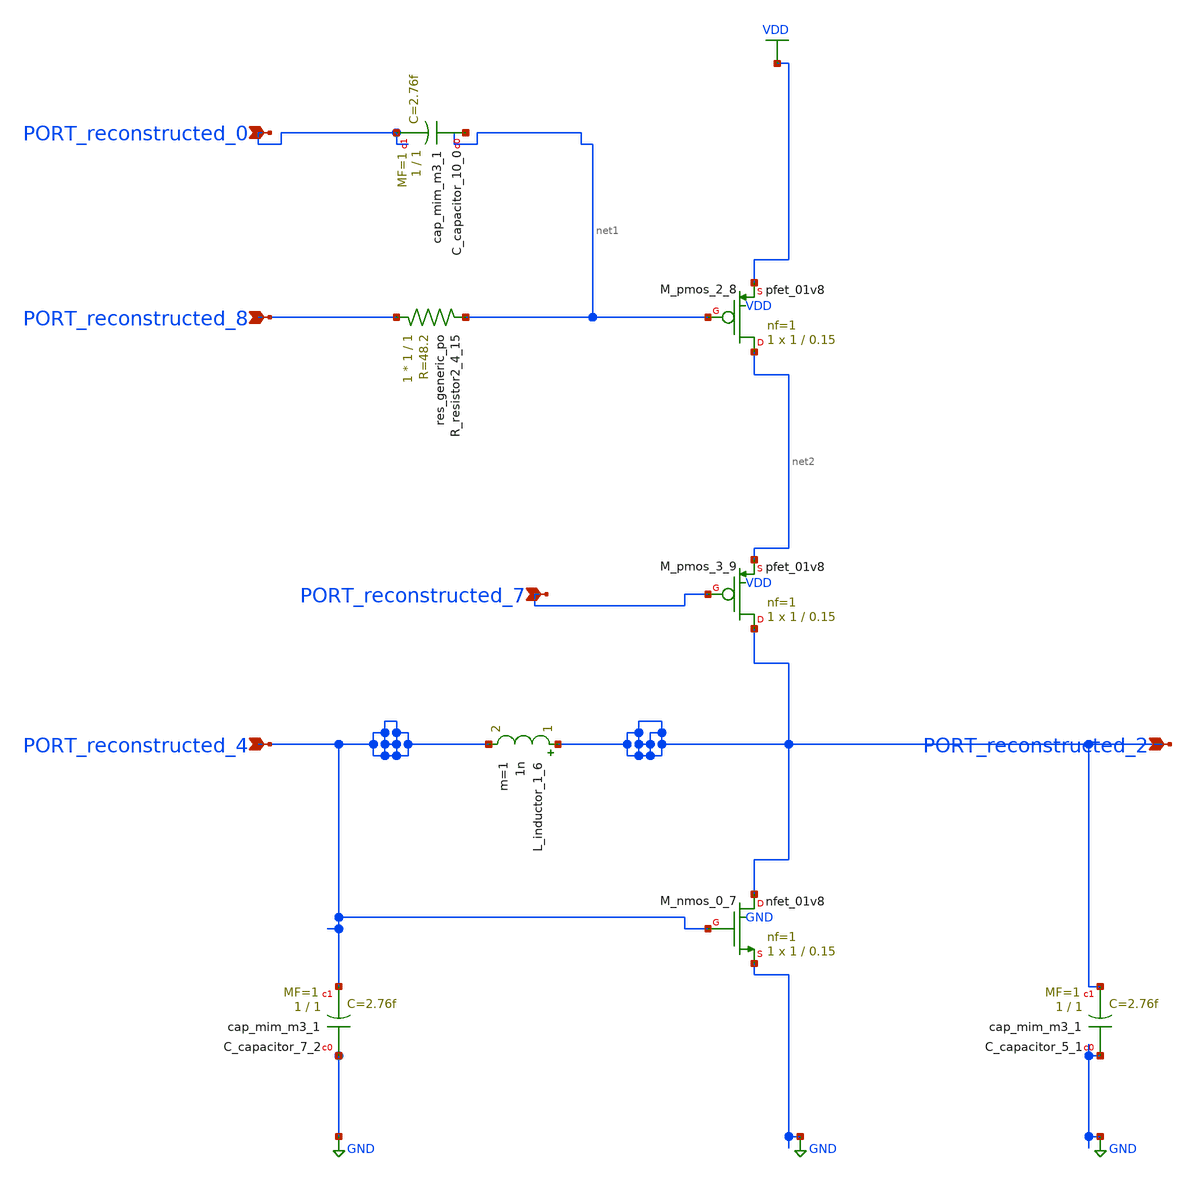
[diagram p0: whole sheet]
** sch_path: schematics/SchemGen/10_1109_ACCESS_2020_2989192_07_006.sch
**.subckt 10_1109_ACCESS_2020_2989192_07_006 PORT_reconstructed_7 PORT_reconstructed_2
*+ PORT_reconstructed_4 PORT_reconstructed_0 PORT_reconstructed_8
*.ipin PORT_reconstructed_7
*.ipin PORT_reconstructed_2
*.ipin PORT_reconstructed_4
*.ipin PORT_reconstructed_0
*.ipin PORT_reconstructed_8
XC_capacitor_10_0 net1 PORT_reconstructed_0 sky130_fd_pr__cap_mim_m3_1 W=1 L=1 MF=1 m=1
XC_capacitor_5_1 GND PORT_reconstructed_2 sky130_fd_pr__cap_mim_m3_1 W=1 L=1 MF=1 m=1
XC_capacitor_7_2 GND PORT_reconstructed_4 sky130_fd_pr__cap_mim_m3_1 W=1 L=1 MF=1 m=1
L_inductor_1_6 PORT_reconstructed_2 PORT_reconstructed_4 1n m=1
XM_nmos_0_7 PORT_reconstructed_2 PORT_reconstructed_4 GND GND sky130_fd_pr__nfet_01v8 L=0.15 W=1 nf=1
+ ad='int((1 + 1)/2) * 1 / 1 * 0.29' as='int((1 + 2)/2) * 1 / 1 * 0.29' pd='2*int((1 + 1)/2) * (1 / 1 + 0.29)'
+ ps='2*int((1 + 2)/2) * (1 / 1 + 0.29)' nrd='0.29 / 1 ' nrs='0.29 / 1 ' sa=0 sb=0 sd=0 mult=1 m=1
XM_pmos_2_8 net2 net1 VDD VDD sky130_fd_pr__pfet_01v8 L=0.15 W=1 nf=1 ad='int((1 + 1)/2) * 1 / 1 * 0.29'
+ as='int((1 + 2)/2) * 1 / 1 * 0.29' pd='2*int((1 + 1)/2) * (1 / 1 + 0.29)' ps='2*int((1 + 2)/2) * (1 / 1 + 0.29)'
+ nrd='0.29 / 1 ' nrs='0.29 / 1 ' sa=0 sb=0 sd=0 mult=1 m=1
XM_pmos_3_9 PORT_reconstructed_2 PORT_reconstructed_7 net2 VDD sky130_fd_pr__pfet_01v8 L=0.15 W=1 nf=1
+ ad='int((1 + 1)/2) * 1 / 1 * 0.29' as='int((1 + 2)/2) * 1 / 1 * 0.29' pd='2*int((1 + 1)/2) * (1 / 1 + 0.29)'
+ ps='2*int((1 + 2)/2) * (1 / 1 + 0.29)' nrd='0.29 / 1 ' nrs='0.29 / 1 ' sa=0 sb=0 sd=0 mult=1 m=1
XR_resistor2_4_15 PORT_reconstructed_8 net1 sky130_fd_pr__res_generic_po W=1 L=1 m=1
**.ends
.GLOBAL GND
.GLOBAL VDD
.end
